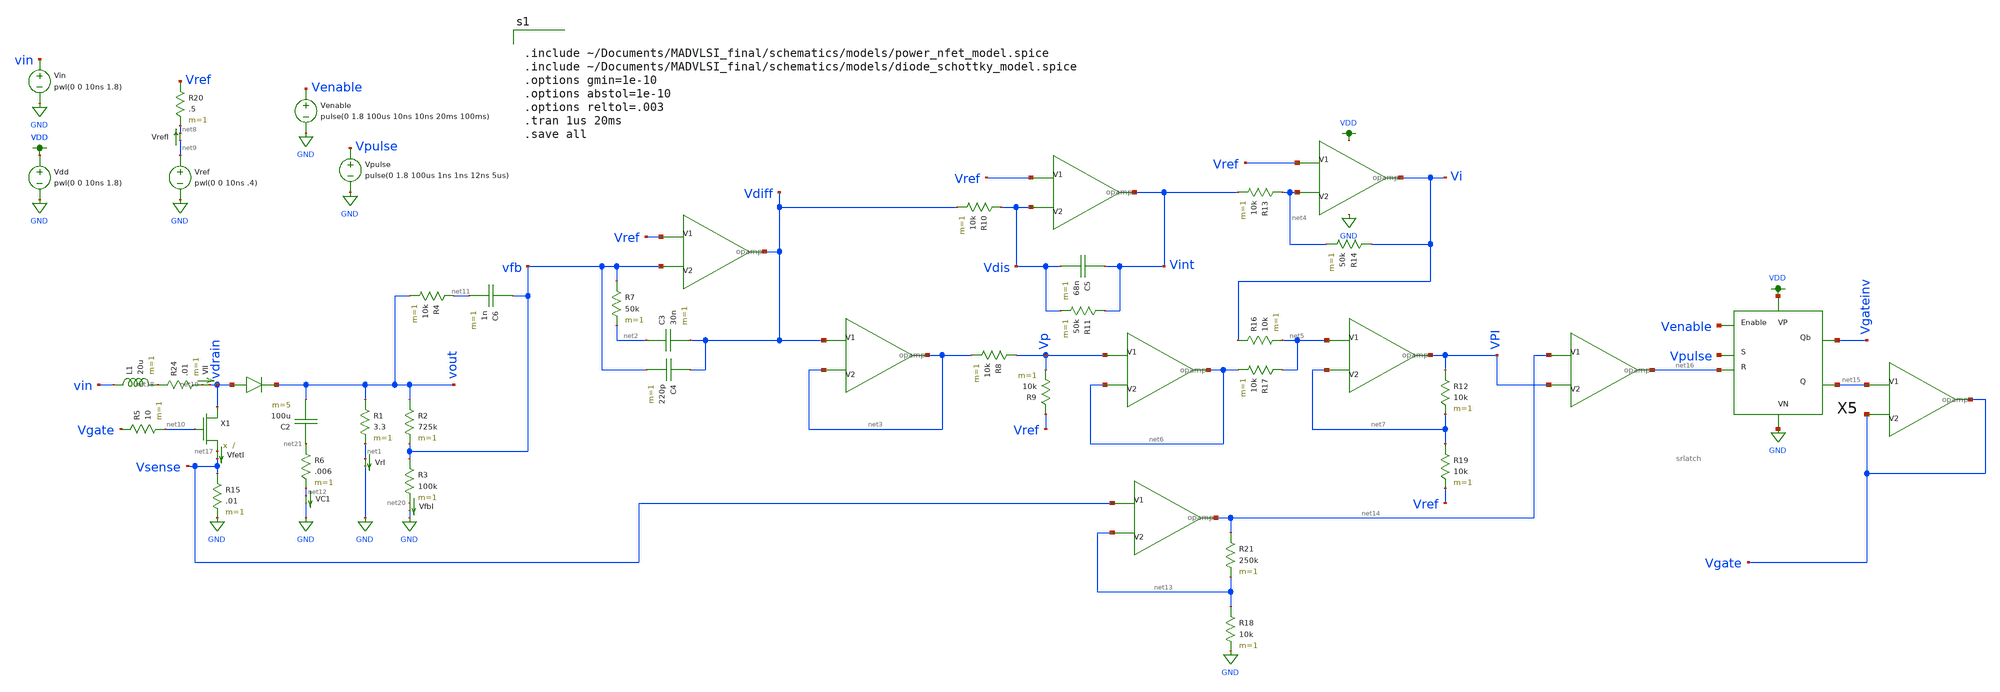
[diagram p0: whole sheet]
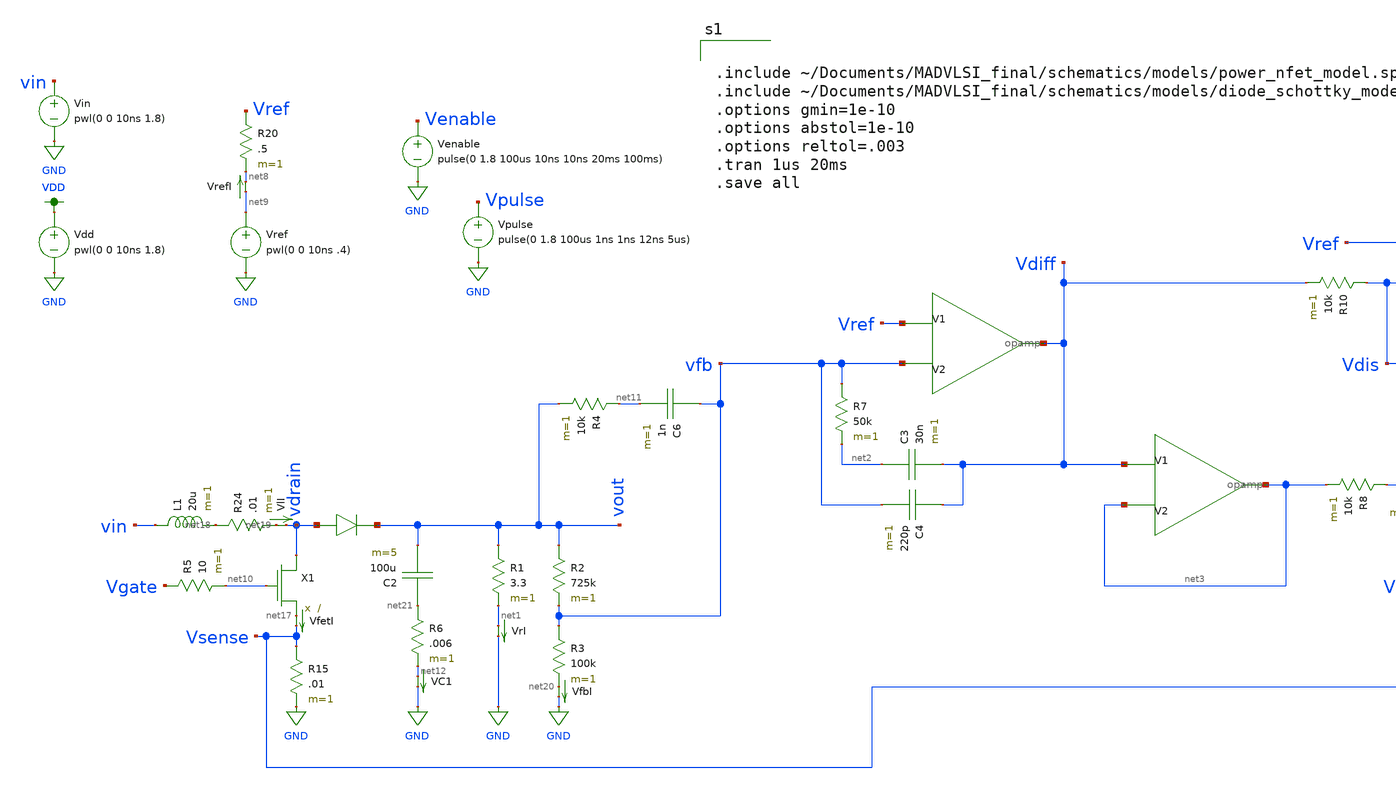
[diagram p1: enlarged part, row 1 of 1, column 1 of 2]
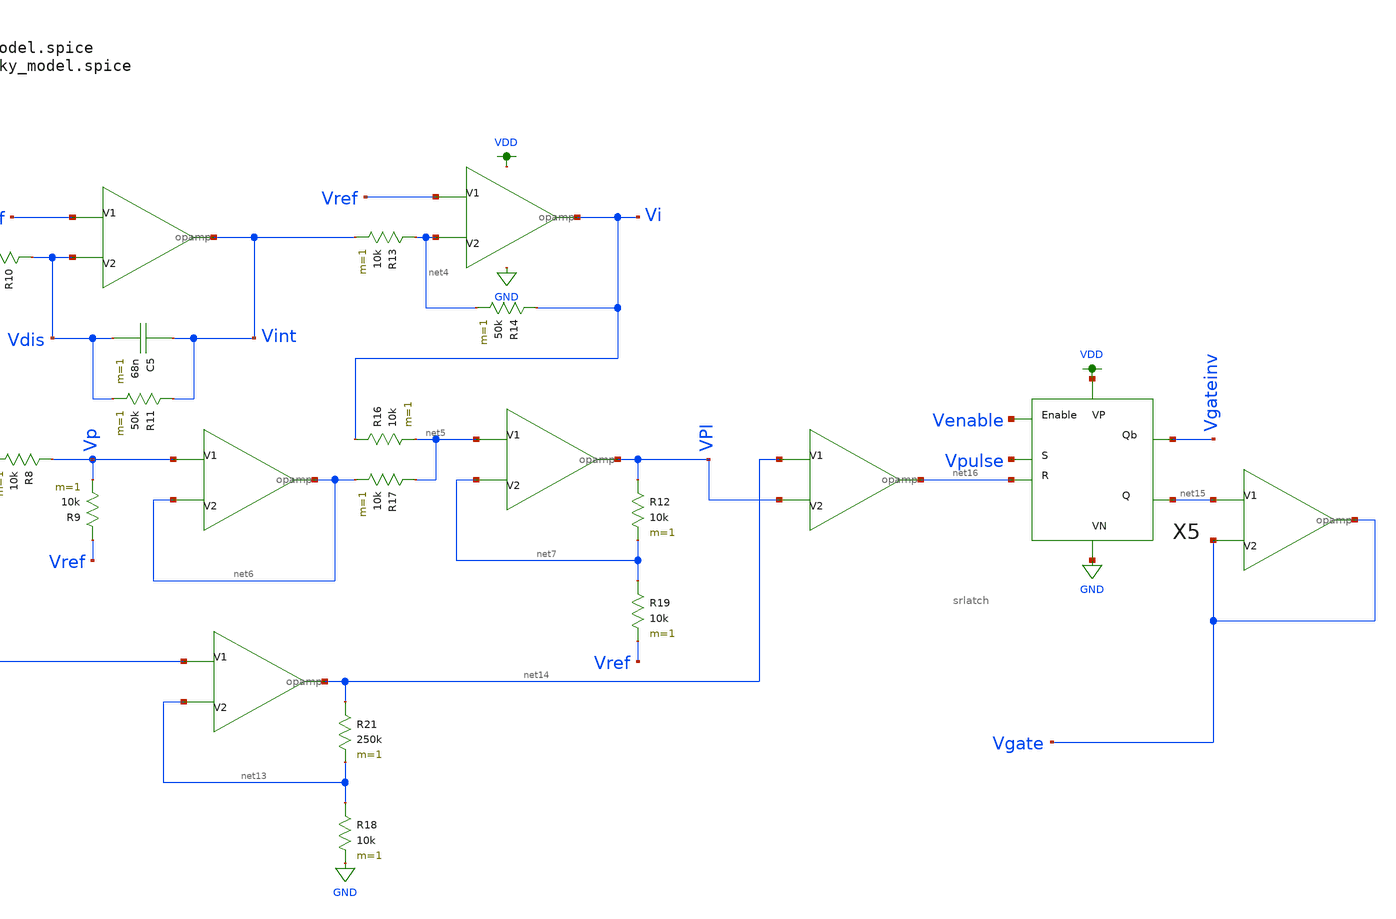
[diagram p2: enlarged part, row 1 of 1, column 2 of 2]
** sch_path: schematics/boost_CMC_tmp.sch
**.subckt boost_CMC_tmp
Vin vin GND pwl(0 0 10ns 1.8)
VfetI net17 Vsense 0
.save i(vfeti)
X1 vdrain net10 net17 power_nfet
L1 vin net18 20u m=1
D1 vdrain vout diode_schottky
R1 vout net1 3.3 m=1
VlI net19 vdrain 0
.save i(vli)
VrI net1 GND 0
.save i(vri)
R2 vout vfb 725k m=1
R3 vfb net20 100k m=1
Vdd VDD GND pwl(0 0 10ns 1.8)
Vref net9 GND pwl(0 0 10ns .4)
R7 vfb net2 50k m=1
X3 Vref vfb Vdiff opamp
X4 Vdiff net3 net3 opamp
R8 Vp net3 10k m=1
R9 Vref Vp 10k m=1
X6 Vref Vdis Vint opamp
R10 Vdis Vdiff 10k m=1
C5 Vint Vdis 68n m=1
R11 Vint Vdis 50k m=1
X7 Vref net4 Vi opamp
R13 net4 Vint 10k m=1
R14 Vi net4 50k m=1
X8 net5 net7 VPI opamp
R16 Vi net5 10k m=1
R17 net5 net6 10k m=1
X9 Vp net6 net6 opamp
R19 net7 Vref 10k m=1
X11 net14 VPI net16 opamp
Vpulse Vpulse GND pulse(0 1.8 100us 1ns 1ns 12ns 5us)
VrefI net9 net8 0
.save i(vrefi)
R24 net18 net19 .01 m=1
VfbI net20 GND 0
.save i(vfbi)
R20 Vref net8 .5 m=1
R12 VPI net7 10k m=1
C3 net2 Vdiff 30n m=1
C4 Vdiff vfb 220p m=1
R4 net11 vout 10k m=1
C6 vfb net11 1n m=1
R5 Vgate net10 10 m=1
C2 net21 vout 100u m=5
R6 net21 net12 .006 m=1
VC1 net12 GND 0
.save i(vc1)
R15 Vsense GND .01 m=1
X2 Vsense net13 net14 opamp
R18 net13 GND 10k m=1
R21 net14 net13 250k m=1
X5 Venable Vpulse net16 VDD GND Vgateinv net15 srlatch
X10 net15 Vgate Vgate opamp
Venable Venable GND pulse(0 1.8 100us 10ns 10ns 20ms 100ms)
**** begin user architecture code


.include ~/Documents/MADVLSI_final/schematics/models/power_nfet_model.spice
.include ~/Documents/MADVLSI_final/schematics/models/diode_schottky_model.spice
.options gmin=1e-10
.options abstol=1e-10
.options reltol=.003
.tran 1us 20ms
.save all


.option wnflag=1
.lib ~/skywater/skywater-pdk/libraries/sky130_fd_pr_ngspice/latest/models/sky130.lib.spice tt

**** end user architecture code
**.ends

* expanding   symbol:  /home/madvlsi/Documents/MADVLSI_final/schematics/opamp.sym # of pins=3
** sym_path: schematics/opamp.sym
** sch_path: schematics/opamp.sch
.subckt opamp V1 V2 VOUT
*.ipin V1
*.ipin V2
*.opin VOUT
XM19 net12 net10 GND VDD sky130_fd_pr__pfet_01v8 L=.6 W=1.5 nf=1 ad='int((nf+1)/2) * W/nf * 0.29' as='int((nf+2)/2) * W/nf * 0.29'
+ pd='2*int((nf+1)/2) * (W/nf + 0.29)' ps='2*int((nf+2)/2) * (W/nf + 0.29)' nrd='0.29 / W' nrs='0.29 / W'
+ sa=0 sb=0 sd=0 mult=1 m=1
XMD20 VDD VDD net12 VDD sky130_fd_pr__pfet_01v8 L=.6 W=1.5 nf=1 ad='int((nf+1)/2) * W/nf * 0.29' as='int((nf+2)/2) * W/nf * 0.29'
+ pd='2*int((nf+1)/2) * (W/nf + 0.29)' ps='2*int((nf+2)/2) * (W/nf + 0.29)' nrd='0.29 / W' nrs='0.29 / W'
+ sa=0 sb=0 sd=0 mult=1 m=1
XM22 net12 net10 net9 VDD sky130_fd_pr__pfet_01v8 L=.6 W=1.5 nf=1 ad='int((nf+1)/2) * W/nf * 0.29' as='int((nf+2)/2) * W/nf * 0.29'
+ pd='2*int((nf+1)/2) * (W/nf + 0.29)' ps='2*int((nf+2)/2) * (W/nf + 0.29)' nrd='0.29 / W' nrs='0.29 / W'
+ sa=0 sb=0 sd=0 mult=1 m=1
XM23 GND net10 net12 VDD sky130_fd_pr__pfet_01v8 L=.6 W=1.5 nf=1 ad='int((nf+1)/2) * W/nf * 0.29' as='int((nf+2)/2) * W/nf * 0.29'
+ pd='2*int((nf+1)/2) * (W/nf + 0.29)' ps='2*int((nf+2)/2) * (W/nf + 0.29)' nrd='0.29 / W' nrs='0.29 / W'
+ sa=0 sb=0 sd=0 mult=1 m=1
XMD24 net9 VDD net10 VDD sky130_fd_pr__pfet_01v8 L=.6 W=1.5 nf=1 ad='int((nf+1)/2) * W/nf * 0.29' as='int((nf+2)/2) * W/nf * 0.29'
+ pd='2*int((nf+1)/2) * (W/nf + 0.29)' ps='2*int((nf+2)/2) * (W/nf + 0.29)' nrd='0.29 / W' nrs='0.29 / W'
+ sa=0 sb=0 sd=0 mult=1 m=1
XM25 VDD net10 net12 VDD sky130_fd_pr__pfet_01v8 L=.6 W=1.5 nf=1 ad='int((nf+1)/2) * W/nf * 0.29' as='int((nf+2)/2) * W/nf * 0.29'
+ pd='2*int((nf+1)/2) * (W/nf + 0.29)' ps='2*int((nf+2)/2) * (W/nf + 0.29)' nrd='0.29 / W' nrs='0.29 / W'
+ sa=0 sb=0 sd=0 mult=1 m=1
XM26 net7 V2 net11 VDD sky130_fd_pr__pfet_01v8 L=.6 W=1.5 nf=1 ad='int((nf+1)/2) * W/nf * 0.29' as='int((nf+2)/2) * W/nf * 0.29'
+ pd='2*int((nf+1)/2) * (W/nf + 0.29)' ps='2*int((nf+2)/2) * (W/nf + 0.29)' nrd='0.29 / W' nrs='0.29 / W'
+ sa=0 sb=0 sd=0 mult=1 m=1
XMD27 net5 VDD net14 VDD sky130_fd_pr__pfet_01v8 L=.6 W=1.5 nf=1 ad='int((nf+1)/2) * W/nf * 0.29' as='int((nf+2)/2) * W/nf * 0.29'
+ pd='2*int((nf+1)/2) * (W/nf + 0.29)' ps='2*int((nf+2)/2) * (W/nf + 0.29)' nrd='0.29 / W' nrs='0.29 / W'
+ sa=0 sb=0 sd=0 mult=1 m=1
XM28 net6 V1 net11 VDD sky130_fd_pr__pfet_01v8 L=.6 W=1.5 nf=1 ad='int((nf+1)/2) * W/nf * 0.29' as='int((nf+2)/2) * W/nf * 0.29'
+ pd='2*int((nf+1)/2) * (W/nf + 0.29)' ps='2*int((nf+2)/2) * (W/nf + 0.29)' nrd='0.29 / W' nrs='0.29 / W'
+ sa=0 sb=0 sd=0 mult=1 m=1
XM29 net11 net10 VDD VDD sky130_fd_pr__pfet_01v8 L=.6 W=1.5 nf=1 ad='int((nf+1)/2) * W/nf * 0.29' as='int((nf+2)/2) * W/nf * 0.29'
+ pd='2*int((nf+1)/2) * (W/nf + 0.29)' ps='2*int((nf+2)/2) * (W/nf + 0.29)' nrd='0.29 / W' nrs='0.29 / W'
+ sa=0 sb=0 sd=0 mult=1 m=1
XMD30 net11 VDD VDD VDD sky130_fd_pr__pfet_01v8 L=.6 W=1.5 nf=1 ad='int((nf+1)/2) * W/nf * 0.29' as='int((nf+2)/2) * W/nf * 0.29'
+ pd='2*int((nf+1)/2) * (W/nf + 0.29)' ps='2*int((nf+2)/2) * (W/nf + 0.29)' nrd='0.29 / W' nrs='0.29 / W'
+ sa=0 sb=0 sd=0 mult=1 m=1
XMD31 net2 VDD net13 VDD sky130_fd_pr__pfet_01v8 L=.6 W=1.5 nf=1 ad='int((nf+1)/2) * W/nf * 0.29' as='int((nf+2)/2) * W/nf * 0.29'
+ pd='2*int((nf+1)/2) * (W/nf + 0.29)' ps='2*int((nf+2)/2) * (W/nf + 0.29)' nrd='0.29 / W' nrs='0.29 / W'
+ sa=0 sb=0 sd=0 mult=1 m=1
XM32 net4 net5 net5 VDD sky130_fd_pr__pfet_01v8 L=.6 W=1.5 nf=1 ad='int((nf+1)/2) * W/nf * 0.29' as='int((nf+2)/2) * W/nf * 0.29'
+ pd='2*int((nf+1)/2) * (W/nf + 0.29)' ps='2*int((nf+2)/2) * (W/nf + 0.29)' nrd='0.29 / W' nrs='0.29 / W'
+ sa=0 sb=0 sd=0 mult=1 m=1
XM33 VDD net10 net4 VDD sky130_fd_pr__pfet_01v8 L=.6 W=1.5 nf=1 ad='int((nf+1)/2) * W/nf * 0.29' as='int((nf+2)/2) * W/nf * 0.29'
+ pd='2*int((nf+1)/2) * (W/nf + 0.29)' ps='2*int((nf+2)/2) * (W/nf + 0.29)' nrd='0.29 / W' nrs='0.29 / W'
+ sa=0 sb=0 sd=0 mult=1 m=1
XM34 net3 net5 net2 VDD sky130_fd_pr__pfet_01v8 L=.6 W=1.5 nf=1 ad='int((nf+1)/2) * W/nf * 0.29' as='int((nf+2)/2) * W/nf * 0.29'
+ pd='2*int((nf+1)/2) * (W/nf + 0.29)' ps='2*int((nf+2)/2) * (W/nf + 0.29)' nrd='0.29 / W' nrs='0.29 / W'
+ sa=0 sb=0 sd=0 mult=1 m=1
XM35 VDD net10 net3 VDD sky130_fd_pr__pfet_01v8 L=.6 W=1.5 nf=1 ad='int((nf+1)/2) * W/nf * 0.29' as='int((nf+2)/2) * W/nf * 0.29'
+ pd='2*int((nf+1)/2) * (W/nf + 0.29)' ps='2*int((nf+2)/2) * (W/nf + 0.29)' nrd='0.29 / W' nrs='0.29 / W'
+ sa=0 sb=0 sd=0 mult=1 m=1
XM36 VOUT net2 VDD VDD sky130_fd_pr__pfet_01v8 L=.6 W=1.5 nf=1 ad='int((nf+1)/2) * W/nf * 0.29' as='int((nf+2)/2) * W/nf * 0.29'
+ pd='2*int((nf+1)/2) * (W/nf + 0.29)' ps='2*int((nf+2)/2) * (W/nf + 0.29)' nrd='0.29 / W' nrs='0.29 / W'
+ sa=0 sb=0 sd=0 mult=1 m=1
XM37 VDD net2 VOUT VDD sky130_fd_pr__pfet_01v8 L=.6 W=1.5 nf=1 ad='int((nf+1)/2) * W/nf * 0.29' as='int((nf+2)/2) * W/nf * 0.29'
+ pd='2*int((nf+1)/2) * (W/nf + 0.29)' ps='2*int((nf+2)/2) * (W/nf + 0.29)' nrd='0.29 / W' nrs='0.29 / W'
+ sa=0 sb=0 sd=0 mult=1 m=1
XM38 VOUT net2 VDD VDD sky130_fd_pr__pfet_01v8 L=.6 W=1.5 nf=1 ad='int((nf+1)/2) * W/nf * 0.29' as='int((nf+2)/2) * W/nf * 0.29'
+ pd='2*int((nf+1)/2) * (W/nf + 0.29)' ps='2*int((nf+2)/2) * (W/nf + 0.29)' nrd='0.29 / W' nrs='0.29 / W'
+ sa=0 sb=0 sd=0 mult=1 m=1
XM39 VDD net2 VOUT VDD sky130_fd_pr__pfet_01v8 L=.6 W=1.5 nf=1 ad='int((nf+1)/2) * W/nf * 0.29' as='int((nf+2)/2) * W/nf * 0.29'
+ pd='2*int((nf+1)/2) * (W/nf + 0.29)' ps='2*int((nf+2)/2) * (W/nf + 0.29)' nrd='0.29 / W' nrs='0.29 / W'
+ sa=0 sb=0 sd=0 mult=1 m=1
XM40 net1 net9 VDD GND sky130_fd_pr__nfet_01v8 L=.6 W=1.5 nf=1 ad='int((nf+1)/2) * W/nf * 0.29' as='int((nf+2)/2) * W/nf * 0.29'
+ pd='2*int((nf+1)/2) * (W/nf + 0.29)' ps='2*int((nf+2)/2) * (W/nf + 0.29)' nrd='0.29 / W' nrs='0.29 / W'
+ sa=0 sb=0 sd=0 mult=1 m=1
XMD41 GND GND net1 GND sky130_fd_pr__nfet_01v8 L=.6 W=1.5 nf=1 ad='int((nf+1)/2) * W/nf * 0.29' as='int((nf+2)/2) * W/nf * 0.29'
+ pd='2*int((nf+1)/2) * (W/nf + 0.29)' ps='2*int((nf+2)/2) * (W/nf + 0.29)' nrd='0.29 / W' nrs='0.29 / W'
+ sa=0 sb=0 sd=0 mult=1 m=1
XM42 net1 net9 net10 GND sky130_fd_pr__nfet_01v8 L=.6 W=1.5 nf=1 ad='int((nf+1)/2) * W/nf * 0.29' as='int((nf+2)/2) * W/nf * 0.29'
+ pd='2*int((nf+1)/2) * (W/nf + 0.29)' ps='2*int((nf+2)/2) * (W/nf + 0.29)' nrd='0.29 / W' nrs='0.29 / W'
+ sa=0 sb=0 sd=0 mult=1 m=1
XM43 VDD net9 net1 GND sky130_fd_pr__nfet_01v8 L=.6 W=1.5 nf=1 ad='int((nf+1)/2) * W/nf * 0.29' as='int((nf+2)/2) * W/nf * 0.29'
+ pd='2*int((nf+1)/2) * (W/nf + 0.29)' ps='2*int((nf+2)/2) * (W/nf + 0.29)' nrd='0.29 / W' nrs='0.29 / W'
+ sa=0 sb=0 sd=0 mult=1 m=1
XMD44 net10 GND net9 GND sky130_fd_pr__nfet_01v8 L=.6 W=1.5 nf=1 ad='int((nf+1)/2) * W/nf * 0.29' as='int((nf+2)/2) * W/nf * 0.29'
+ pd='2*int((nf+1)/2) * (W/nf + 0.29)' ps='2*int((nf+2)/2) * (W/nf + 0.29)' nrd='0.29 / W' nrs='0.29 / W'
+ sa=0 sb=0 sd=0 mult=1 m=1
XM45 GND net9 net1 GND sky130_fd_pr__nfet_01v8 L=.6 W=1.5 nf=1 ad='int((nf+1)/2) * W/nf * 0.29' as='int((nf+2)/2) * W/nf * 0.29'
+ pd='2*int((nf+1)/2) * (W/nf + 0.29)' ps='2*int((nf+2)/2) * (W/nf + 0.29)' nrd='0.29 / W' nrs='0.29 / W'
+ sa=0 sb=0 sd=0 mult=1 m=1
XM46 net3 V1 net8 GND sky130_fd_pr__nfet_01v8 L=.6 W=1.5 nf=1 ad='int((nf+1)/2) * W/nf * 0.29' as='int((nf+2)/2) * W/nf * 0.29'
+ pd='2*int((nf+1)/2) * (W/nf + 0.29)' ps='2*int((nf+2)/2) * (W/nf + 0.29)' nrd='0.29 / W' nrs='0.29 / W'
+ sa=0 sb=0 sd=0 mult=1 m=1
XMD47 net5 GND net15 GND sky130_fd_pr__nfet_01v8 L=.6 W=1.5 nf=1 ad='int((nf+1)/2) * W/nf * 0.29' as='int((nf+2)/2) * W/nf * 0.29'
+ pd='2*int((nf+1)/2) * (W/nf + 0.29)' ps='2*int((nf+2)/2) * (W/nf + 0.29)' nrd='0.29 / W' nrs='0.29 / W'
+ sa=0 sb=0 sd=0 mult=1 m=1
XM48 net4 V2 net8 GND sky130_fd_pr__nfet_01v8 L=.6 W=1.5 nf=1 ad='int((nf+1)/2) * W/nf * 0.29' as='int((nf+2)/2) * W/nf * 0.29'
+ pd='2*int((nf+1)/2) * (W/nf + 0.29)' ps='2*int((nf+2)/2) * (W/nf + 0.29)' nrd='0.29 / W' nrs='0.29 / W'
+ sa=0 sb=0 sd=0 mult=1 m=1
XM49 net8 net9 GND GND sky130_fd_pr__nfet_01v8 L=.6 W=1.5 nf=1 ad='int((nf+1)/2) * W/nf * 0.29' as='int((nf+2)/2) * W/nf * 0.29'
+ pd='2*int((nf+1)/2) * (W/nf + 0.29)' ps='2*int((nf+2)/2) * (W/nf + 0.29)' nrd='0.29 / W' nrs='0.29 / W'
+ sa=0 sb=0 sd=0 mult=1 m=1
XMD50 net8 GND GND GND sky130_fd_pr__nfet_01v8 L=.6 W=1.5 nf=1 ad='int((nf+1)/2) * W/nf * 0.29' as='int((nf+2)/2) * W/nf * 0.29'
+ pd='2*int((nf+1)/2) * (W/nf + 0.29)' ps='2*int((nf+2)/2) * (W/nf + 0.29)' nrd='0.29 / W' nrs='0.29 / W'
+ sa=0 sb=0 sd=0 mult=1 m=1
XMD51 net2 GND net16 GND sky130_fd_pr__nfet_01v8 L=.6 W=1.5 nf=1 ad='int((nf+1)/2) * W/nf * 0.29' as='int((nf+2)/2) * W/nf * 0.29'
+ pd='2*int((nf+1)/2) * (W/nf + 0.29)' ps='2*int((nf+2)/2) * (W/nf + 0.29)' nrd='0.29 / W' nrs='0.29 / W'
+ sa=0 sb=0 sd=0 mult=1 m=1
XM52 GND net9 net7 GND sky130_fd_pr__nfet_01v8 L=.6 W=1.5 nf=1 ad='int((nf+1)/2) * W/nf * 0.29' as='int((nf+2)/2) * W/nf * 0.29'
+ pd='2*int((nf+1)/2) * (W/nf + 0.29)' ps='2*int((nf+2)/2) * (W/nf + 0.29)' nrd='0.29 / W' nrs='0.29 / W'
+ sa=0 sb=0 sd=0 mult=1 m=1
XMD53 VOUT GND GND GND sky130_fd_pr__nfet_01v8 L=.6 W=1.5 nf=1 ad='int((nf+1)/2) * W/nf * 0.29' as='int((nf+2)/2) * W/nf * 0.29'
+ pd='2*int((nf+1)/2) * (W/nf + 0.29)' ps='2*int((nf+2)/2) * (W/nf + 0.29)' nrd='0.29 / W' nrs='0.29 / W'
+ sa=0 sb=0 sd=0 mult=1 m=1
XM54 GND net9 net6 GND sky130_fd_pr__nfet_01v8 L=.6 W=1.5 nf=1 ad='int((nf+1)/2) * W/nf * 0.29' as='int((nf+2)/2) * W/nf * 0.29'
+ pd='2*int((nf+1)/2) * (W/nf + 0.29)' ps='2*int((nf+2)/2) * (W/nf + 0.29)' nrd='0.29 / W' nrs='0.29 / W'
+ sa=0 sb=0 sd=0 mult=1 m=1
XM55 net7 net5 net5 GND sky130_fd_pr__nfet_01v8 L=.6 W=1.5 nf=1 ad='int((nf+1)/2) * W/nf * 0.29' as='int((nf+2)/2) * W/nf * 0.29'
+ pd='2*int((nf+1)/2) * (W/nf + 0.29)' ps='2*int((nf+2)/2) * (W/nf + 0.29)' nrd='0.29 / W' nrs='0.29 / W'
+ sa=0 sb=0 sd=0 mult=1 m=1
XM56 net6 net5 net2 GND sky130_fd_pr__nfet_01v8 L=.6 W=1.5 nf=1 ad='int((nf+1)/2) * W/nf * 0.29' as='int((nf+2)/2) * W/nf * 0.29'
+ pd='2*int((nf+1)/2) * (W/nf + 0.29)' ps='2*int((nf+2)/2) * (W/nf + 0.29)' nrd='0.29 / W' nrs='0.29 / W'
+ sa=0 sb=0 sd=0 mult=1 m=1
XMD57 VOUT GND GND GND sky130_fd_pr__nfet_01v8 L=.6 W=1.5 nf=1 ad='int((nf+1)/2) * W/nf * 0.29' as='int((nf+2)/2) * W/nf * 0.29'
+ pd='2*int((nf+1)/2) * (W/nf + 0.29)' ps='2*int((nf+2)/2) * (W/nf + 0.29)' nrd='0.29 / W' nrs='0.29 / W'
+ sa=0 sb=0 sd=0 mult=1 m=1
XM58 GND net2 VOUT GND sky130_fd_pr__nfet_01v8 L=.6 W=1.5 nf=1 ad='int((nf+1)/2) * W/nf * 0.29' as='int((nf+2)/2) * W/nf * 0.29'
+ pd='2*int((nf+1)/2) * (W/nf + 0.29)' ps='2*int((nf+2)/2) * (W/nf + 0.29)' nrd='0.29 / W' nrs='0.29 / W'
+ sa=0 sb=0 sd=0 mult=1 m=1
XM59 GND net2 VOUT GND sky130_fd_pr__nfet_01v8 L=.6 W=1.5 nf=1 ad='int((nf+1)/2) * W/nf * 0.29' as='int((nf+2)/2) * W/nf * 0.29'
+ pd='2*int((nf+1)/2) * (W/nf + 0.29)' ps='2*int((nf+2)/2) * (W/nf + 0.29)' nrd='0.29 / W' nrs='0.29 / W'
+ sa=0 sb=0 sd=0 mult=1 m=1
XM60 net12 net10 GND VDD sky130_fd_pr__pfet_01v8 L=.6 W=1.5 nf=1 ad='int((nf+1)/2) * W/nf * 0.29' as='int((nf+2)/2) * W/nf * 0.29'
+ pd='2*int((nf+1)/2) * (W/nf + 0.29)' ps='2*int((nf+2)/2) * (W/nf + 0.29)' nrd='0.29 / W' nrs='0.29 / W'
+ sa=0 sb=0 sd=0 mult=1 m=1
XM61 net10 net10 net4 VDD sky130_fd_pr__pfet_01v8 L=.6 W=1.5 nf=1 ad='int((nf+1)/2) * W/nf * 0.29' as='int((nf+2)/2) * W/nf * 0.29'
+ pd='2*int((nf+1)/2) * (W/nf + 0.29)' ps='2*int((nf+2)/2) * (W/nf + 0.29)' nrd='0.29 / W' nrs='0.29 / W'
+ sa=0 sb=0 sd=0 mult=1 m=1
XM62 net1 net9 VDD GND sky130_fd_pr__nfet_01v8 L=.6 W=1.5 nf=1 ad='int((nf+1)/2) * W/nf * 0.29' as='int((nf+2)/2) * W/nf * 0.29'
+ pd='2*int((nf+1)/2) * (W/nf + 0.29)' ps='2*int((nf+2)/2) * (W/nf + 0.29)' nrd='0.29 / W' nrs='0.29 / W'
+ sa=0 sb=0 sd=0 mult=1 m=1
XM63 net9 net9 net7 GND sky130_fd_pr__nfet_01v8 L=.6 W=1.5 nf=1 ad='int((nf+1)/2) * W/nf * 0.29' as='int((nf+2)/2) * W/nf * 0.29'
+ pd='2*int((nf+1)/2) * (W/nf + 0.29)' ps='2*int((nf+2)/2) * (W/nf + 0.29)' nrd='0.29 / W' nrs='0.29 / W'
+ sa=0 sb=0 sd=0 mult=1 m=1
XMD64 VDD GND GND GND sky130_fd_pr__nfet_01v8 L=.6 W=1.5 nf=1 ad='int((nf+1)/2) * W/nf * 0.29' as='int((nf+2)/2) * W/nf * 0.29'
+ pd='2*int((nf+1)/2) * (W/nf + 0.29)' ps='2*int((nf+2)/2) * (W/nf + 0.29)' nrd='0.29 / W' nrs='0.29 / W'
+ sa=0 sb=0 sd=0 mult=1 m=1
XMD65 net7 GND GND GND sky130_fd_pr__nfet_01v8 L=.6 W=1.5 nf=1 ad='int((nf+1)/2) * W/nf * 0.29' as='int((nf+2)/2) * W/nf * 0.29'
+ pd='2*int((nf+1)/2) * (W/nf + 0.29)' ps='2*int((nf+2)/2) * (W/nf + 0.29)' nrd='0.29 / W' nrs='0.29 / W'
+ sa=0 sb=0 sd=0 mult=1 m=1
XMD66 GND VDD VDD VDD sky130_fd_pr__pfet_01v8 L=.6 W=1.5 nf=1 ad='int((nf+1)/2) * W/nf * 0.29' as='int((nf+2)/2) * W/nf * 0.29'
+ pd='2*int((nf+1)/2) * (W/nf + 0.29)' ps='2*int((nf+2)/2) * (W/nf + 0.29)' nrd='0.29 / W' nrs='0.29 / W'
+ sa=0 sb=0 sd=0 mult=1 m=1
XMD67 net4 VDD VDD VDD sky130_fd_pr__pfet_01v8 L=.6 W=1.5 nf=1 ad='int((nf+1)/2) * W/nf * 0.29' as='int((nf+2)/2) * W/nf * 0.29'
+ pd='2*int((nf+1)/2) * (W/nf + 0.29)' ps='2*int((nf+2)/2) * (W/nf + 0.29)' nrd='0.29 / W' nrs='0.29 / W'
+ sa=0 sb=0 sd=0 mult=1 m=1
XMD1 net15 GND net3 GND sky130_fd_pr__nfet_01v8 L=.6 W=1.5 nf=1 ad='int((nf+1)/2) * W/nf * 0.29' as='int((nf+2)/2) * W/nf * 0.29'
+ pd='2*int((nf+1)/2) * (W/nf + 0.29)' ps='2*int((nf+2)/2) * (W/nf + 0.29)' nrd='0.29 / W' nrs='0.29 / W'
+ sa=0 sb=0 sd=0 mult=1 m=1
XMD2 net16 GND net4 GND sky130_fd_pr__nfet_01v8 L=.6 W=1.5 nf=1 ad='int((nf+1)/2) * W/nf * 0.29' as='int((nf+2)/2) * W/nf * 0.29'
+ pd='2*int((nf+1)/2) * (W/nf + 0.29)' ps='2*int((nf+2)/2) * (W/nf + 0.29)' nrd='0.29 / W' nrs='0.29 / W'
+ sa=0 sb=0 sd=0 mult=1 m=1
XMD3 net13 VDD net6 VDD sky130_fd_pr__pfet_01v8 L=.6 W=1.5 nf=1 ad='int((nf+1)/2) * W/nf * 0.29' as='int((nf+2)/2) * W/nf * 0.29'
+ pd='2*int((nf+1)/2) * (W/nf + 0.29)' ps='2*int((nf+2)/2) * (W/nf + 0.29)' nrd='0.29 / W' nrs='0.29 / W'
+ sa=0 sb=0 sd=0 mult=1 m=1
XMD4 net14 VDD net7 VDD sky130_fd_pr__pfet_01v8 L=.6 W=1.5 nf=1 ad='int((nf+1)/2) * W/nf * 0.29' as='int((nf+2)/2) * W/nf * 0.29'
+ pd='2*int((nf+1)/2) * (W/nf + 0.29)' ps='2*int((nf+2)/2) * (W/nf + 0.29)' nrd='0.29 / W' nrs='0.29 / W'
+ sa=0 sb=0 sd=0 mult=1 m=1
XM1 net21 net10 GND VDD sky130_fd_pr__pfet_01v8 L=.6 W=1.5 nf=1 ad='int((nf+1)/2) * W/nf * 0.29' as='int((nf+2)/2) * W/nf * 0.29'
+ pd='2*int((nf+1)/2) * (W/nf + 0.29)' ps='2*int((nf+2)/2) * (W/nf + 0.29)' nrd='0.29 / W' nrs='0.29 / W'
+ sa=0 sb=0 sd=0 mult=1 m=1
XMD5 VDD VDD net21 VDD sky130_fd_pr__pfet_01v8 L=.6 W=1.5 nf=1 ad='int((nf+1)/2) * W/nf * 0.29' as='int((nf+2)/2) * W/nf * 0.29'
+ pd='2*int((nf+1)/2) * (W/nf + 0.29)' ps='2*int((nf+2)/2) * (W/nf + 0.29)' nrd='0.29 / W' nrs='0.29 / W'
+ sa=0 sb=0 sd=0 mult=1 m=1
XM6 net21 net10 net9 VDD sky130_fd_pr__pfet_01v8 L=.6 W=1.5 nf=1 ad='int((nf+1)/2) * W/nf * 0.29' as='int((nf+2)/2) * W/nf * 0.29'
+ pd='2*int((nf+1)/2) * (W/nf + 0.29)' ps='2*int((nf+2)/2) * (W/nf + 0.29)' nrd='0.29 / W' nrs='0.29 / W'
+ sa=0 sb=0 sd=0 mult=1 m=1
XM7 GND net10 net21 VDD sky130_fd_pr__pfet_01v8 L=.6 W=1.5 nf=1 ad='int((nf+1)/2) * W/nf * 0.29' as='int((nf+2)/2) * W/nf * 0.29'
+ pd='2*int((nf+1)/2) * (W/nf + 0.29)' ps='2*int((nf+2)/2) * (W/nf + 0.29)' nrd='0.29 / W' nrs='0.29 / W'
+ sa=0 sb=0 sd=0 mult=1 m=1
XMD8 net9 VDD net10 VDD sky130_fd_pr__pfet_01v8 L=.6 W=1.5 nf=1 ad='int((nf+1)/2) * W/nf * 0.29' as='int((nf+2)/2) * W/nf * 0.29'
+ pd='2*int((nf+1)/2) * (W/nf + 0.29)' ps='2*int((nf+2)/2) * (W/nf + 0.29)' nrd='0.29 / W' nrs='0.29 / W'
+ sa=0 sb=0 sd=0 mult=1 m=1
XM9 VDD net10 net21 VDD sky130_fd_pr__pfet_01v8 L=.6 W=1.5 nf=1 ad='int((nf+1)/2) * W/nf * 0.29' as='int((nf+2)/2) * W/nf * 0.29'
+ pd='2*int((nf+1)/2) * (W/nf + 0.29)' ps='2*int((nf+2)/2) * (W/nf + 0.29)' nrd='0.29 / W' nrs='0.29 / W'
+ sa=0 sb=0 sd=0 mult=1 m=1
XM10 net7 V2 net20 VDD sky130_fd_pr__pfet_01v8 L=.6 W=1.5 nf=1 ad='int((nf+1)/2) * W/nf * 0.29' as='int((nf+2)/2) * W/nf * 0.29'
+ pd='2*int((nf+1)/2) * (W/nf + 0.29)' ps='2*int((nf+2)/2) * (W/nf + 0.29)' nrd='0.29 / W' nrs='0.29 / W'
+ sa=0 sb=0 sd=0 mult=1 m=1
XMD11 net18 VDD net23 VDD sky130_fd_pr__pfet_01v8 L=.6 W=1.5 nf=1 ad='int((nf+1)/2) * W/nf * 0.29' as='int((nf+2)/2) * W/nf * 0.29'
+ pd='2*int((nf+1)/2) * (W/nf + 0.29)' ps='2*int((nf+2)/2) * (W/nf + 0.29)' nrd='0.29 / W' nrs='0.29 / W'
+ sa=0 sb=0 sd=0 mult=1 m=1
XM12 net6 V1 net20 VDD sky130_fd_pr__pfet_01v8 L=.6 W=1.5 nf=1 ad='int((nf+1)/2) * W/nf * 0.29' as='int((nf+2)/2) * W/nf * 0.29'
+ pd='2*int((nf+1)/2) * (W/nf + 0.29)' ps='2*int((nf+2)/2) * (W/nf + 0.29)' nrd='0.29 / W' nrs='0.29 / W'
+ sa=0 sb=0 sd=0 mult=1 m=1
XM13 net20 net10 VDD VDD sky130_fd_pr__pfet_01v8 L=.6 W=1.5 nf=1 ad='int((nf+1)/2) * W/nf * 0.29' as='int((nf+2)/2) * W/nf * 0.29'
+ pd='2*int((nf+1)/2) * (W/nf + 0.29)' ps='2*int((nf+2)/2) * (W/nf + 0.29)' nrd='0.29 / W' nrs='0.29 / W'
+ sa=0 sb=0 sd=0 mult=1 m=1
XMD14 net20 VDD VDD VDD sky130_fd_pr__pfet_01v8 L=.6 W=1.5 nf=1 ad='int((nf+1)/2) * W/nf * 0.29' as='int((nf+2)/2) * W/nf * 0.29'
+ pd='2*int((nf+1)/2) * (W/nf + 0.29)' ps='2*int((nf+2)/2) * (W/nf + 0.29)' nrd='0.29 / W' nrs='0.29 / W'
+ sa=0 sb=0 sd=0 mult=1 m=1
XMD15 net2 VDD net22 VDD sky130_fd_pr__pfet_01v8 L=.6 W=1.5 nf=1 ad='int((nf+1)/2) * W/nf * 0.29' as='int((nf+2)/2) * W/nf * 0.29'
+ pd='2*int((nf+1)/2) * (W/nf + 0.29)' ps='2*int((nf+2)/2) * (W/nf + 0.29)' nrd='0.29 / W' nrs='0.29 / W'
+ sa=0 sb=0 sd=0 mult=1 m=1
XM16 net4 net18 net18 VDD sky130_fd_pr__pfet_01v8 L=.6 W=1.5 nf=1 ad='int((nf+1)/2) * W/nf * 0.29' as='int((nf+2)/2) * W/nf * 0.29'
+ pd='2*int((nf+1)/2) * (W/nf + 0.29)' ps='2*int((nf+2)/2) * (W/nf + 0.29)' nrd='0.29 / W' nrs='0.29 / W'
+ sa=0 sb=0 sd=0 mult=1 m=1
XM17 VDD net10 net4 VDD sky130_fd_pr__pfet_01v8 L=.6 W=1.5 nf=1 ad='int((nf+1)/2) * W/nf * 0.29' as='int((nf+2)/2) * W/nf * 0.29'
+ pd='2*int((nf+1)/2) * (W/nf + 0.29)' ps='2*int((nf+2)/2) * (W/nf + 0.29)' nrd='0.29 / W' nrs='0.29 / W'
+ sa=0 sb=0 sd=0 mult=1 m=1
XM18 net3 net18 net2 VDD sky130_fd_pr__pfet_01v8 L=.6 W=1.5 nf=1 ad='int((nf+1)/2) * W/nf * 0.29' as='int((nf+2)/2) * W/nf * 0.29'
+ pd='2*int((nf+1)/2) * (W/nf + 0.29)' ps='2*int((nf+2)/2) * (W/nf + 0.29)' nrd='0.29 / W' nrs='0.29 / W'
+ sa=0 sb=0 sd=0 mult=1 m=1
XM20 VDD net10 net3 VDD sky130_fd_pr__pfet_01v8 L=.6 W=1.5 nf=1 ad='int((nf+1)/2) * W/nf * 0.29' as='int((nf+2)/2) * W/nf * 0.29'
+ pd='2*int((nf+1)/2) * (W/nf + 0.29)' ps='2*int((nf+2)/2) * (W/nf + 0.29)' nrd='0.29 / W' nrs='0.29 / W'
+ sa=0 sb=0 sd=0 mult=1 m=1
XM21 VOUT net2 VDD VDD sky130_fd_pr__pfet_01v8 L=.6 W=1.5 nf=1 ad='int((nf+1)/2) * W/nf * 0.29' as='int((nf+2)/2) * W/nf * 0.29'
+ pd='2*int((nf+1)/2) * (W/nf + 0.29)' ps='2*int((nf+2)/2) * (W/nf + 0.29)' nrd='0.29 / W' nrs='0.29 / W'
+ sa=0 sb=0 sd=0 mult=1 m=1
XM24 VDD net2 VOUT VDD sky130_fd_pr__pfet_01v8 L=.6 W=1.5 nf=1 ad='int((nf+1)/2) * W/nf * 0.29' as='int((nf+2)/2) * W/nf * 0.29'
+ pd='2*int((nf+1)/2) * (W/nf + 0.29)' ps='2*int((nf+2)/2) * (W/nf + 0.29)' nrd='0.29 / W' nrs='0.29 / W'
+ sa=0 sb=0 sd=0 mult=1 m=1
XM27 VOUT net2 VDD VDD sky130_fd_pr__pfet_01v8 L=.6 W=1.5 nf=1 ad='int((nf+1)/2) * W/nf * 0.29' as='int((nf+2)/2) * W/nf * 0.29'
+ pd='2*int((nf+1)/2) * (W/nf + 0.29)' ps='2*int((nf+2)/2) * (W/nf + 0.29)' nrd='0.29 / W' nrs='0.29 / W'
+ sa=0 sb=0 sd=0 mult=1 m=1
XM30 VDD net2 VOUT VDD sky130_fd_pr__pfet_01v8 L=.6 W=1.5 nf=1 ad='int((nf+1)/2) * W/nf * 0.29' as='int((nf+2)/2) * W/nf * 0.29'
+ pd='2*int((nf+1)/2) * (W/nf + 0.29)' ps='2*int((nf+2)/2) * (W/nf + 0.29)' nrd='0.29 / W' nrs='0.29 / W'
+ sa=0 sb=0 sd=0 mult=1 m=1
XM31 net17 net9 VDD GND sky130_fd_pr__nfet_01v8 L=.6 W=1.5 nf=1 ad='int((nf+1)/2) * W/nf * 0.29' as='int((nf+2)/2) * W/nf * 0.29'
+ pd='2*int((nf+1)/2) * (W/nf + 0.29)' ps='2*int((nf+2)/2) * (W/nf + 0.29)' nrd='0.29 / W' nrs='0.29 / W'
+ sa=0 sb=0 sd=0 mult=1 m=1
XMD32 GND GND net17 GND sky130_fd_pr__nfet_01v8 L=.6 W=1.5 nf=1 ad='int((nf+1)/2) * W/nf * 0.29' as='int((nf+2)/2) * W/nf * 0.29'
+ pd='2*int((nf+1)/2) * (W/nf + 0.29)' ps='2*int((nf+2)/2) * (W/nf + 0.29)' nrd='0.29 / W' nrs='0.29 / W'
+ sa=0 sb=0 sd=0 mult=1 m=1
XM41 net17 net9 net10 GND sky130_fd_pr__nfet_01v8 L=.6 W=1.5 nf=1 ad='int((nf+1)/2) * W/nf * 0.29' as='int((nf+2)/2) * W/nf * 0.29'
+ pd='2*int((nf+1)/2) * (W/nf + 0.29)' ps='2*int((nf+2)/2) * (W/nf + 0.29)' nrd='0.29 / W' nrs='0.29 / W'
+ sa=0 sb=0 sd=0 mult=1 m=1
XM44 VDD net9 net17 GND sky130_fd_pr__nfet_01v8 L=.6 W=1.5 nf=1 ad='int((nf+1)/2) * W/nf * 0.29' as='int((nf+2)/2) * W/nf * 0.29'
+ pd='2*int((nf+1)/2) * (W/nf + 0.29)' ps='2*int((nf+2)/2) * (W/nf + 0.29)' nrd='0.29 / W' nrs='0.29 / W'
+ sa=0 sb=0 sd=0 mult=1 m=1
XMD45 net10 GND net9 GND sky130_fd_pr__nfet_01v8 L=.6 W=1.5 nf=1 ad='int((nf+1)/2) * W/nf * 0.29' as='int((nf+2)/2) * W/nf * 0.29'
+ pd='2*int((nf+1)/2) * (W/nf + 0.29)' ps='2*int((nf+2)/2) * (W/nf + 0.29)' nrd='0.29 / W' nrs='0.29 / W'
+ sa=0 sb=0 sd=0 mult=1 m=1
XM47 GND net9 net17 GND sky130_fd_pr__nfet_01v8 L=.6 W=1.5 nf=1 ad='int((nf+1)/2) * W/nf * 0.29' as='int((nf+2)/2) * W/nf * 0.29'
+ pd='2*int((nf+1)/2) * (W/nf + 0.29)' ps='2*int((nf+2)/2) * (W/nf + 0.29)' nrd='0.29 / W' nrs='0.29 / W'
+ sa=0 sb=0 sd=0 mult=1 m=1
XM50 net3 V1 net19 GND sky130_fd_pr__nfet_01v8 L=.6 W=1.5 nf=1 ad='int((nf+1)/2) * W/nf * 0.29' as='int((nf+2)/2) * W/nf * 0.29'
+ pd='2*int((nf+1)/2) * (W/nf + 0.29)' ps='2*int((nf+2)/2) * (W/nf + 0.29)' nrd='0.29 / W' nrs='0.29 / W'
+ sa=0 sb=0 sd=0 mult=1 m=1
XMD52 net18 GND net24 GND sky130_fd_pr__nfet_01v8 L=.6 W=1.5 nf=1 ad='int((nf+1)/2) * W/nf * 0.29' as='int((nf+2)/2) * W/nf * 0.29'
+ pd='2*int((nf+1)/2) * (W/nf + 0.29)' ps='2*int((nf+2)/2) * (W/nf + 0.29)' nrd='0.29 / W' nrs='0.29 / W'
+ sa=0 sb=0 sd=0 mult=1 m=1
XM53 net4 V2 net19 GND sky130_fd_pr__nfet_01v8 L=.6 W=1.5 nf=1 ad='int((nf+1)/2) * W/nf * 0.29' as='int((nf+2)/2) * W/nf * 0.29'
+ pd='2*int((nf+1)/2) * (W/nf + 0.29)' ps='2*int((nf+2)/2) * (W/nf + 0.29)' nrd='0.29 / W' nrs='0.29 / W'
+ sa=0 sb=0 sd=0 mult=1 m=1
XM57 net19 net9 GND GND sky130_fd_pr__nfet_01v8 L=.6 W=1.5 nf=1 ad='int((nf+1)/2) * W/nf * 0.29' as='int((nf+2)/2) * W/nf * 0.29'
+ pd='2*int((nf+1)/2) * (W/nf + 0.29)' ps='2*int((nf+2)/2) * (W/nf + 0.29)' nrd='0.29 / W' nrs='0.29 / W'
+ sa=0 sb=0 sd=0 mult=1 m=1
XMD58 net19 GND GND GND sky130_fd_pr__nfet_01v8 L=.6 W=1.5 nf=1 ad='int((nf+1)/2) * W/nf * 0.29' as='int((nf+2)/2) * W/nf * 0.29'
+ pd='2*int((nf+1)/2) * (W/nf + 0.29)' ps='2*int((nf+2)/2) * (W/nf + 0.29)' nrd='0.29 / W' nrs='0.29 / W'
+ sa=0 sb=0 sd=0 mult=1 m=1
XMD59 net2 GND net25 GND sky130_fd_pr__nfet_01v8 L=.6 W=1.5 nf=1 ad='int((nf+1)/2) * W/nf * 0.29' as='int((nf+2)/2) * W/nf * 0.29'
+ pd='2*int((nf+1)/2) * (W/nf + 0.29)' ps='2*int((nf+2)/2) * (W/nf + 0.29)' nrd='0.29 / W' nrs='0.29 / W'
+ sa=0 sb=0 sd=0 mult=1 m=1
XM64 GND net9 net7 GND sky130_fd_pr__nfet_01v8 L=.6 W=1.5 nf=1 ad='int((nf+1)/2) * W/nf * 0.29' as='int((nf+2)/2) * W/nf * 0.29'
+ pd='2*int((nf+1)/2) * (W/nf + 0.29)' ps='2*int((nf+2)/2) * (W/nf + 0.29)' nrd='0.29 / W' nrs='0.29 / W'
+ sa=0 sb=0 sd=0 mult=1 m=1
XMD68 VOUT GND GND GND sky130_fd_pr__nfet_01v8 L=.6 W=1.5 nf=1 ad='int((nf+1)/2) * W/nf * 0.29' as='int((nf+2)/2) * W/nf * 0.29'
+ pd='2*int((nf+1)/2) * (W/nf + 0.29)' ps='2*int((nf+2)/2) * (W/nf + 0.29)' nrd='0.29 / W' nrs='0.29 / W'
+ sa=0 sb=0 sd=0 mult=1 m=1
XM69 GND net9 net6 GND sky130_fd_pr__nfet_01v8 L=.6 W=1.5 nf=1 ad='int((nf+1)/2) * W/nf * 0.29' as='int((nf+2)/2) * W/nf * 0.29'
+ pd='2*int((nf+1)/2) * (W/nf + 0.29)' ps='2*int((nf+2)/2) * (W/nf + 0.29)' nrd='0.29 / W' nrs='0.29 / W'
+ sa=0 sb=0 sd=0 mult=1 m=1
XM70 net7 net18 net18 GND sky130_fd_pr__nfet_01v8 L=.6 W=1.5 nf=1 ad='int((nf+1)/2) * W/nf * 0.29' as='int((nf+2)/2) * W/nf * 0.29'
+ pd='2*int((nf+1)/2) * (W/nf + 0.29)' ps='2*int((nf+2)/2) * (W/nf + 0.29)' nrd='0.29 / W' nrs='0.29 / W'
+ sa=0 sb=0 sd=0 mult=1 m=1
XM71 net6 net18 net2 GND sky130_fd_pr__nfet_01v8 L=.6 W=1.5 nf=1 ad='int((nf+1)/2) * W/nf * 0.29' as='int((nf+2)/2) * W/nf * 0.29'
+ pd='2*int((nf+1)/2) * (W/nf + 0.29)' ps='2*int((nf+2)/2) * (W/nf + 0.29)' nrd='0.29 / W' nrs='0.29 / W'
+ sa=0 sb=0 sd=0 mult=1 m=1
XMD72 VOUT GND GND GND sky130_fd_pr__nfet_01v8 L=.6 W=1.5 nf=1 ad='int((nf+1)/2) * W/nf * 0.29' as='int((nf+2)/2) * W/nf * 0.29'
+ pd='2*int((nf+1)/2) * (W/nf + 0.29)' ps='2*int((nf+2)/2) * (W/nf + 0.29)' nrd='0.29 / W' nrs='0.29 / W'
+ sa=0 sb=0 sd=0 mult=1 m=1
XM73 GND net2 VOUT GND sky130_fd_pr__nfet_01v8 L=.6 W=1.5 nf=1 ad='int((nf+1)/2) * W/nf * 0.29' as='int((nf+2)/2) * W/nf * 0.29'
+ pd='2*int((nf+1)/2) * (W/nf + 0.29)' ps='2*int((nf+2)/2) * (W/nf + 0.29)' nrd='0.29 / W' nrs='0.29 / W'
+ sa=0 sb=0 sd=0 mult=1 m=1
XM74 GND net2 VOUT GND sky130_fd_pr__nfet_01v8 L=.6 W=1.5 nf=1 ad='int((nf+1)/2) * W/nf * 0.29' as='int((nf+2)/2) * W/nf * 0.29'
+ pd='2*int((nf+1)/2) * (W/nf + 0.29)' ps='2*int((nf+2)/2) * (W/nf + 0.29)' nrd='0.29 / W' nrs='0.29 / W'
+ sa=0 sb=0 sd=0 mult=1 m=1
XM75 net21 net10 GND VDD sky130_fd_pr__pfet_01v8 L=.6 W=1.5 nf=1 ad='int((nf+1)/2) * W/nf * 0.29' as='int((nf+2)/2) * W/nf * 0.29'
+ pd='2*int((nf+1)/2) * (W/nf + 0.29)' ps='2*int((nf+2)/2) * (W/nf + 0.29)' nrd='0.29 / W' nrs='0.29 / W'
+ sa=0 sb=0 sd=0 mult=1 m=1
XM76 net10 net10 net4 VDD sky130_fd_pr__pfet_01v8 L=.6 W=1.5 nf=1 ad='int((nf+1)/2) * W/nf * 0.29' as='int((nf+2)/2) * W/nf * 0.29'
+ pd='2*int((nf+1)/2) * (W/nf + 0.29)' ps='2*int((nf+2)/2) * (W/nf + 0.29)' nrd='0.29 / W' nrs='0.29 / W'
+ sa=0 sb=0 sd=0 mult=1 m=1
XM77 net17 net9 VDD GND sky130_fd_pr__nfet_01v8 L=.6 W=1.5 nf=1 ad='int((nf+1)/2) * W/nf * 0.29' as='int((nf+2)/2) * W/nf * 0.29'
+ pd='2*int((nf+1)/2) * (W/nf + 0.29)' ps='2*int((nf+2)/2) * (W/nf + 0.29)' nrd='0.29 / W' nrs='0.29 / W'
+ sa=0 sb=0 sd=0 mult=1 m=1
XM78 net9 net9 net7 GND sky130_fd_pr__nfet_01v8 L=.6 W=1.5 nf=1 ad='int((nf+1)/2) * W/nf * 0.29' as='int((nf+2)/2) * W/nf * 0.29'
+ pd='2*int((nf+1)/2) * (W/nf + 0.29)' ps='2*int((nf+2)/2) * (W/nf + 0.29)' nrd='0.29 / W' nrs='0.29 / W'
+ sa=0 sb=0 sd=0 mult=1 m=1
XMD79 VDD GND GND GND sky130_fd_pr__nfet_01v8 L=.6 W=1.5 nf=1 ad='int((nf+1)/2) * W/nf * 0.29' as='int((nf+2)/2) * W/nf * 0.29'
+ pd='2*int((nf+1)/2) * (W/nf + 0.29)' ps='2*int((nf+2)/2) * (W/nf + 0.29)' nrd='0.29 / W' nrs='0.29 / W'
+ sa=0 sb=0 sd=0 mult=1 m=1
XMD80 net7 GND GND GND sky130_fd_pr__nfet_01v8 L=.6 W=1.5 nf=1 ad='int((nf+1)/2) * W/nf * 0.29' as='int((nf+2)/2) * W/nf * 0.29'
+ pd='2*int((nf+1)/2) * (W/nf + 0.29)' ps='2*int((nf+2)/2) * (W/nf + 0.29)' nrd='0.29 / W' nrs='0.29 / W'
+ sa=0 sb=0 sd=0 mult=1 m=1
XMD81 GND VDD VDD VDD sky130_fd_pr__pfet_01v8 L=.6 W=1.5 nf=1 ad='int((nf+1)/2) * W/nf * 0.29' as='int((nf+2)/2) * W/nf * 0.29'
+ pd='2*int((nf+1)/2) * (W/nf + 0.29)' ps='2*int((nf+2)/2) * (W/nf + 0.29)' nrd='0.29 / W' nrs='0.29 / W'
+ sa=0 sb=0 sd=0 mult=1 m=1
XMD82 net4 VDD VDD VDD sky130_fd_pr__pfet_01v8 L=.6 W=1.5 nf=1 ad='int((nf+1)/2) * W/nf * 0.29' as='int((nf+2)/2) * W/nf * 0.29'
+ pd='2*int((nf+1)/2) * (W/nf + 0.29)' ps='2*int((nf+2)/2) * (W/nf + 0.29)' nrd='0.29 / W' nrs='0.29 / W'
+ sa=0 sb=0 sd=0 mult=1 m=1
XMD83 net24 GND net3 GND sky130_fd_pr__nfet_01v8 L=.6 W=1.5 nf=1 ad='int((nf+1)/2) * W/nf * 0.29' as='int((nf+2)/2) * W/nf * 0.29'
+ pd='2*int((nf+1)/2) * (W/nf + 0.29)' ps='2*int((nf+2)/2) * (W/nf + 0.29)' nrd='0.29 / W' nrs='0.29 / W'
+ sa=0 sb=0 sd=0 mult=1 m=1
XMD84 net25 GND net4 GND sky130_fd_pr__nfet_01v8 L=.6 W=1.5 nf=1 ad='int((nf+1)/2) * W/nf * 0.29' as='int((nf+2)/2) * W/nf * 0.29'
+ pd='2*int((nf+1)/2) * (W/nf + 0.29)' ps='2*int((nf+2)/2) * (W/nf + 0.29)' nrd='0.29 / W' nrs='0.29 / W'
+ sa=0 sb=0 sd=0 mult=1 m=1
XMD85 net22 VDD net6 VDD sky130_fd_pr__pfet_01v8 L=.6 W=1.5 nf=1 ad='int((nf+1)/2) * W/nf * 0.29' as='int((nf+2)/2) * W/nf * 0.29'
+ pd='2*int((nf+1)/2) * (W/nf + 0.29)' ps='2*int((nf+2)/2) * (W/nf + 0.29)' nrd='0.29 / W' nrs='0.29 / W'
+ sa=0 sb=0 sd=0 mult=1 m=1
XMD86 net23 VDD net7 VDD sky130_fd_pr__pfet_01v8 L=.6 W=1.5 nf=1 ad='int((nf+1)/2) * W/nf * 0.29' as='int((nf+2)/2) * W/nf * 0.29'
+ pd='2*int((nf+1)/2) * (W/nf + 0.29)' ps='2*int((nf+2)/2) * (W/nf + 0.29)' nrd='0.29 / W' nrs='0.29 / W'
+ sa=0 sb=0 sd=0 mult=1 m=1
XC1 net2 VOUT sky130_fd_pr__cap_mim_m3_1 W=20 L=12 MF=1 m=1
.ends


* expanding   symbol:  srlatch.sym # of pins=7
** sym_path: schematics/srlatch.sym
** sch_path: schematics/srlatch.sch
.subckt srlatch Enable S R VP VN Qb Q
*.ipin S
*.ipin R
*.iopin VP
*.iopin VN
*.opin Q
*.opin Qb
*.ipin Enable
X1 net1 Q VP VN Qb nor
X2 Qb net2 VP VN Q nor
X3 S Enable VP VN net1 and
X4 Enable R VP VN net2 and
.ends


* expanding   symbol:  /home/madvlsi/Documents/MADVLSI_final/schematics/nor.sym # of pins=5
** sym_path: schematics/nor.sym
** sch_path: schematics/nor.sch
.subckt nor A B VP VN Z
*.ipin A
*.ipin B
*.iopin VP
*.iopin VN
*.opin Z
**** begin user architecture code

.param l=.15
.param w=1

**** end user architecture code
XM1 Z A VN GND sky130_fd_pr__nfet_01v8 L=l W=w nf=1 ad='int((nf+1)/2) * W/nf * 0.29' as='int((nf+2)/2) * W/nf * 0.29'
+ pd='2*int((nf+1)/2) * (W/nf + 0.29)' ps='2*int((nf+2)/2) * (W/nf + 0.29)' nrd='0.29 / W' nrs='0.29 / W'
+ sa=0 sb=0 sd=0 mult=1 m=1
XM2 VN B Z GND sky130_fd_pr__nfet_01v8 L=l W=w nf=1 ad='int((nf+1)/2) * W/nf * 0.29' as='int((nf+2)/2) * W/nf * 0.29'
+ pd='2*int((nf+1)/2) * (W/nf + 0.29)' ps='2*int((nf+2)/2) * (W/nf + 0.29)' nrd='0.29 / W' nrs='0.29 / W'
+ sa=0 sb=0 sd=0 mult=1 m=1
XM3 Z A net1 VDD sky130_fd_pr__pfet_01v8 L=l W=w nf=1 ad='int((nf+1)/2) * W/nf * 0.29' as='int((nf+2)/2) * W/nf * 0.29'
+ pd='2*int((nf+1)/2) * (W/nf + 0.29)' ps='2*int((nf+2)/2) * (W/nf + 0.29)' nrd='0.29 / W' nrs='0.29 / W'
+ sa=0 sb=0 sd=0 mult=1 m=1
XM4 VP B net1 VDD sky130_fd_pr__pfet_01v8 L=l W=w nf=1 ad='int((nf+1)/2) * W/nf * 0.29' as='int((nf+2)/2) * W/nf * 0.29'
+ pd='2*int((nf+1)/2) * (W/nf + 0.29)' ps='2*int((nf+2)/2) * (W/nf + 0.29)' nrd='0.29 / W' nrs='0.29 / W'
+ sa=0 sb=0 sd=0 mult=1 m=1
.ends


* expanding   symbol:  /home/madvlsi/Documents/MADVLSI_final/schematics/and.sym # of pins=6
** sym_path: schematics/and.sym
** sch_path: schematics/and.sch
.subckt and A B VP VN Z
*.ipin A
*.ipin B
*.iopin VP
*.iopin VN
*.opin Z
X1 net1 VP VN Z inverter
X2 A B VP VN net1 nand
**** begin user architecture code

.param l=.15
.param w=1
.param mn=1
.param mp=1

**** end user architecture code
.ends


* expanding   symbol:  /home/madvlsi/Documents/final/xschem/inverter.sym # of pins=4
** sym_path: schematics/inverter.sym
** sch_path: schematics/inverter.sch
.subckt inverter A VP VN Z
*.ipin A
*.iopin VP
*.iopin VN
*.opin Z
XM1 Z A VN GND sky130_fd_pr__nfet_01v8 L=0.15 W=1 nf=1 ad='int((nf+1)/2) * W/nf * 0.29' as='int((nf+2)/2) * W/nf * 0.29'
+ pd='2*int((nf+1)/2) * (W/nf + 0.29)' ps='2*int((nf+2)/2) * (W/nf + 0.29)' nrd='0.29 / W' nrs='0.29 / W'
+ sa=0 sb=0 sd=0 mult=1 m=1
XM2 Z A VP VDD sky130_fd_pr__pfet_01v8 L=0.15 W=1 nf=1 ad='int((nf+1)/2) * W/nf * 0.29' as='int((nf+2)/2) * W/nf * 0.29'
+ pd='2*int((nf+1)/2) * (W/nf + 0.29)' ps='2*int((nf+2)/2) * (W/nf + 0.29)' nrd='0.29 / W' nrs='0.29 / W'
+ sa=0 sb=0 sd=0 mult=2 m=2
**** begin user architecture code

.param l=.15
.param w=1
.param mn=1
.param mp=1

**** end user architecture code
.ends


* expanding   symbol:  /home/madvlsi/Documents/final/xschem/nand.sym # of pins=6
** sym_path: schematics/nand.sym
** sch_path: schematics/nand.sch
.subckt nand A B VP VN Z
*.ipin A
*.iopin VP
*.iopin VN
*.opin Z
*.ipin B
XM1 Z A net1 GND sky130_fd_pr__nfet_01v8 L=0.15 W=1 nf=1 ad='int((nf+1)/2) * W/nf * 0.29' as='int((nf+2)/2) * W/nf * 0.29'
+ pd='2*int((nf+1)/2) * (W/nf + 0.29)' ps='2*int((nf+2)/2) * (W/nf + 0.29)' nrd='0.29 / W' nrs='0.29 / W'
+ sa=0 sb=0 sd=0 mult=1 m=1
XM2 VP B Z VDD sky130_fd_pr__pfet_01v8 L=0.15 W=1 nf=1 ad='int((nf+1)/2) * W/nf * 0.29' as='int((nf+2)/2) * W/nf * 0.29'
+ pd='2*int((nf+1)/2) * (W/nf + 0.29)' ps='2*int((nf+2)/2) * (W/nf + 0.29)' nrd='0.29 / W' nrs='0.29 / W'
+ sa=0 sb=0 sd=0 mult=2 m=2
XM3 VN B net1 GND sky130_fd_pr__nfet_01v8 L=0.15 W=1 nf=1 ad='int((nf+1)/2) * W/nf * 0.29' as='int((nf+2)/2) * W/nf * 0.29'
+ pd='2*int((nf+1)/2) * (W/nf + 0.29)' ps='2*int((nf+2)/2) * (W/nf + 0.29)' nrd='0.29 / W' nrs='0.29 / W'
+ sa=0 sb=0 sd=0 mult=1 m=1
XM4 Z A VP VDD sky130_fd_pr__pfet_01v8 L=0.15 W=1 nf=1 ad='int((nf+1)/2) * W/nf * 0.29' as='int((nf+2)/2) * W/nf * 0.29'
+ pd='2*int((nf+1)/2) * (W/nf + 0.29)' ps='2*int((nf+2)/2) * (W/nf + 0.29)' nrd='0.29 / W' nrs='0.29 / W'
+ sa=0 sb=0 sd=0 mult=2 m=2
.ends

.GLOBAL GND
.GLOBAL VDD
.end
